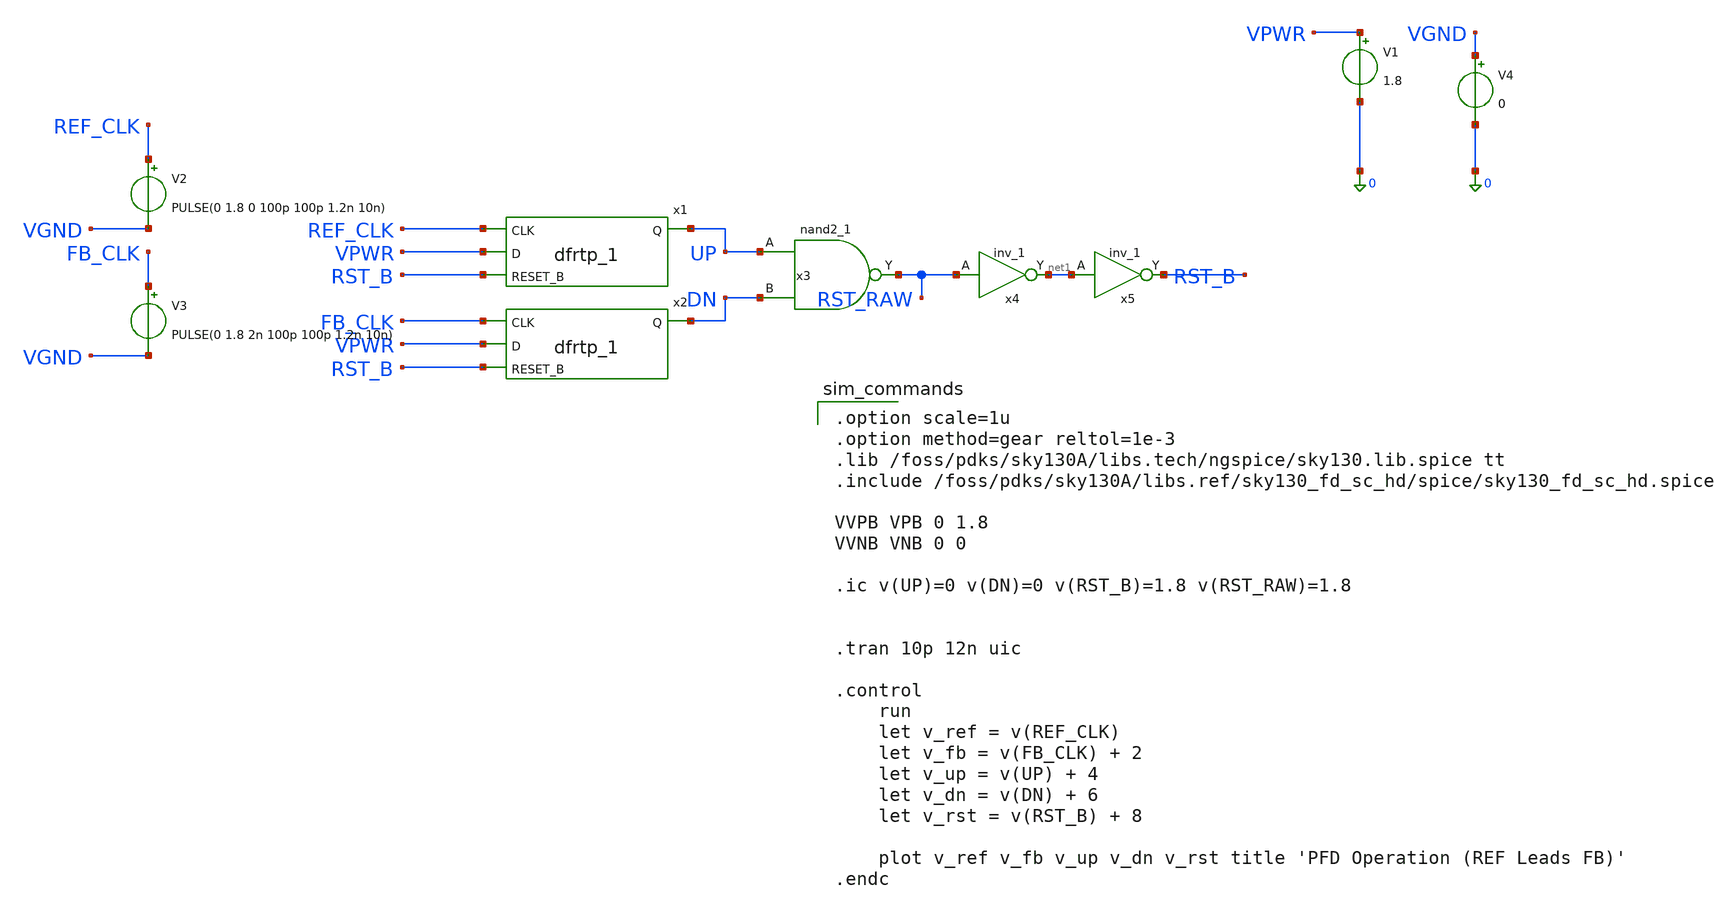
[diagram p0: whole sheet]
** sch_path: pfd_tb.sch
**.subckt pfd_tb
x1 REF_CLK VPWR RST_B VGND VNB VPB VPWR UP sky130_fd_sc_hd__dfrtp_1
x2 FB_CLK VPWR RST_B VGND VNB VPB VPWR DN sky130_fd_sc_hd__dfrtp_1
x3 UP DN VGND VNB VPB VPWR RST_RAW sky130_fd_sc_hd__nand2_1
V2 REF_CLK VGND PULSE(0 1.8 0 100p 100p 1.2n 10n)
V3 FB_CLK VGND PULSE(0 1.8 2n 100p 100p 1.2n 10n)
V1 VPWR 0 1.8
V4 VGND 0 0
x4 RST_RAW VGND VNB VPB VPWR net1 sky130_fd_sc_hd__inv_1
x5 net1 VGND VNB VPB VPWR RST_B sky130_fd_sc_hd__inv_1
**** begin user architecture code

.option scale=1u
.option method=gear reltol=1e-3
.lib /foss/pdks/sky130A/libs.tech/ngspice/sky130.lib.spice tt
.include /foss/pdks/sky130A/libs.ref/sky130_fd_sc_hd/spice/sky130_fd_sc_hd.spice

VVPB VPB 0 1.8
VVNB VNB 0 0

.ic v(UP)=0 v(DN)=0 v(RST_B)=1.8 v(RST_RAW)=1.8


.tran 10p 12n uic

.control
	run
	let v_ref = v(REF_CLK)
	let v_fb = v(FB_CLK) + 2
	let v_up = v(UP) + 4
	let v_dn = v(DN) + 6
	let v_rst = v(RST_B) + 8

	plot v_ref v_fb v_up v_dn v_rst title 'PFD Operation (REF Leads FB)'
.endc

**** end user architecture code
**.ends
.end
